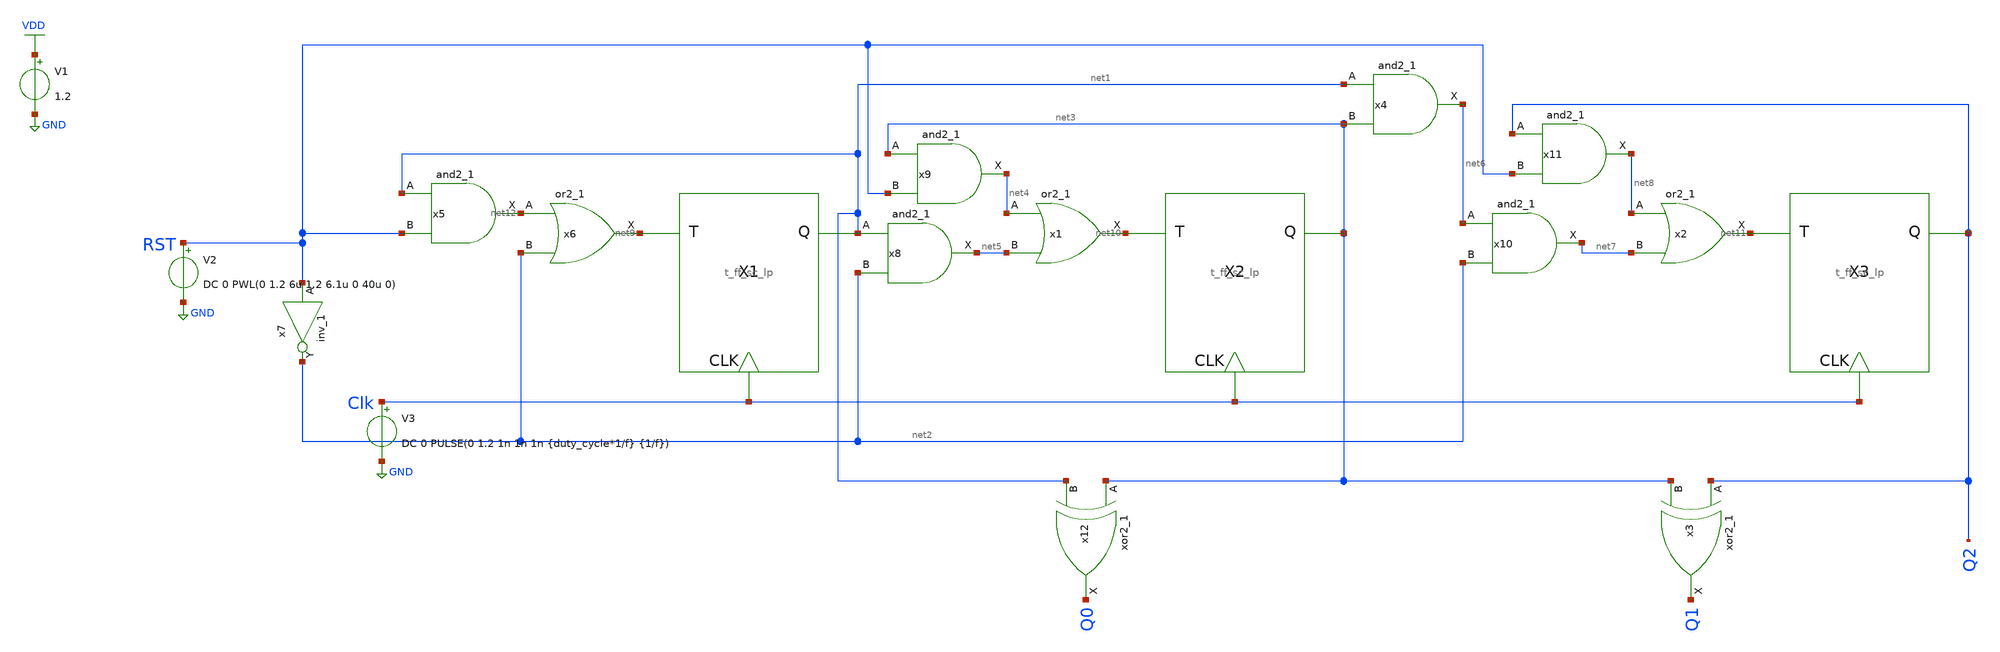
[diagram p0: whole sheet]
** sch_path: xschem/8_bit_gray_counter/3_bit_rst_gray_counter_test.sch
**.subckt 3_bit_rst_gray_counter_test
X1 net9 net1 Clk t_ff_sc_lp
X2 net10 net3 Clk t_ff_sc_lp
X3 net11 Q2 Clk t_ff_sc_lp
x1 net4 net5 GND GND VDD VDD net10 sky130_fd_sc_lp__or2_1
x4 net1 net3 GND GND VDD VDD net6 sky130_fd_sc_lp__and2_1
x5 net1 RST GND GND VDD VDD net12 sky130_fd_sc_lp__and2_1
x6 net12 net2 GND GND VDD VDD net9 sky130_fd_sc_lp__or2_1
x7 RST GND GND VDD VDD net2 sky130_fd_sc_lp__inv_1
x8 net1 net2 GND GND VDD VDD net5 sky130_fd_sc_lp__and2_1
x9 net3 RST GND GND VDD VDD net4 sky130_fd_sc_lp__and2_1
x10 net6 net2 GND GND VDD VDD net7 sky130_fd_sc_lp__and2_1
x11 Q2 RST GND GND VDD VDD net8 sky130_fd_sc_lp__and2_1
x12 net3 net1 GND GND VDD VDD Q0 sky130_fd_sc_lp__xor2_1
x2 net8 net7 GND GND VDD VDD net11 sky130_fd_sc_lp__or2_1
x3 Q2 net3 GND GND VDD VDD Q1 sky130_fd_sc_lp__xor2_1
V1 VDD GND 1.2
V3 Clk GND DC 0 PULSE(0 1.2 1n 1n 1n {duty_cycle*1/f} {1/f})
V2 RST GND DC 0 PWL(0 1.2 6u 1.2 6.1u 0 40u 0)
**** begin user architecture code


.lib /home/sky/sky130A/libs.tech/ngspice/sky130.lib.spice tt
.include /home/sky/sky130A/libs.ref/sky130_fd_sc_lp/spice/sky130_fd_sc_lp.spice
.options abstol=1e-14 reltol=1e-4
.param f=2560k
.param duty_cycle=0.5
*.ic v(Q)=0 v(Q_inv)=1 v(x1.net1)=0
.tran {(1/100)*(1/f)} {40/f}
.save all


**** end user architecture code
**.ends

* expanding   symbol:  T_flip_flop/t_ff_sc_lp.sym # of pins=3
** sym_path: T_flip_flop/t_ff_sc_lp.sym
** sch_path: T_flip_flop/t_ff_sc_lp.sch
.subckt t_ff_sc_lp T Q CLK
*.ipin T
*.ipin CLK
*.opin Q
x3 Q T GND GND VDD VDD net1 sky130_fd_sc_lp__xor2_1
x1 CLK net1 GND GND VDD VDD Q sky130_fd_sc_lp__dfxtp_1
.ends

.GLOBAL VDD
.GLOBAL GND
.end
